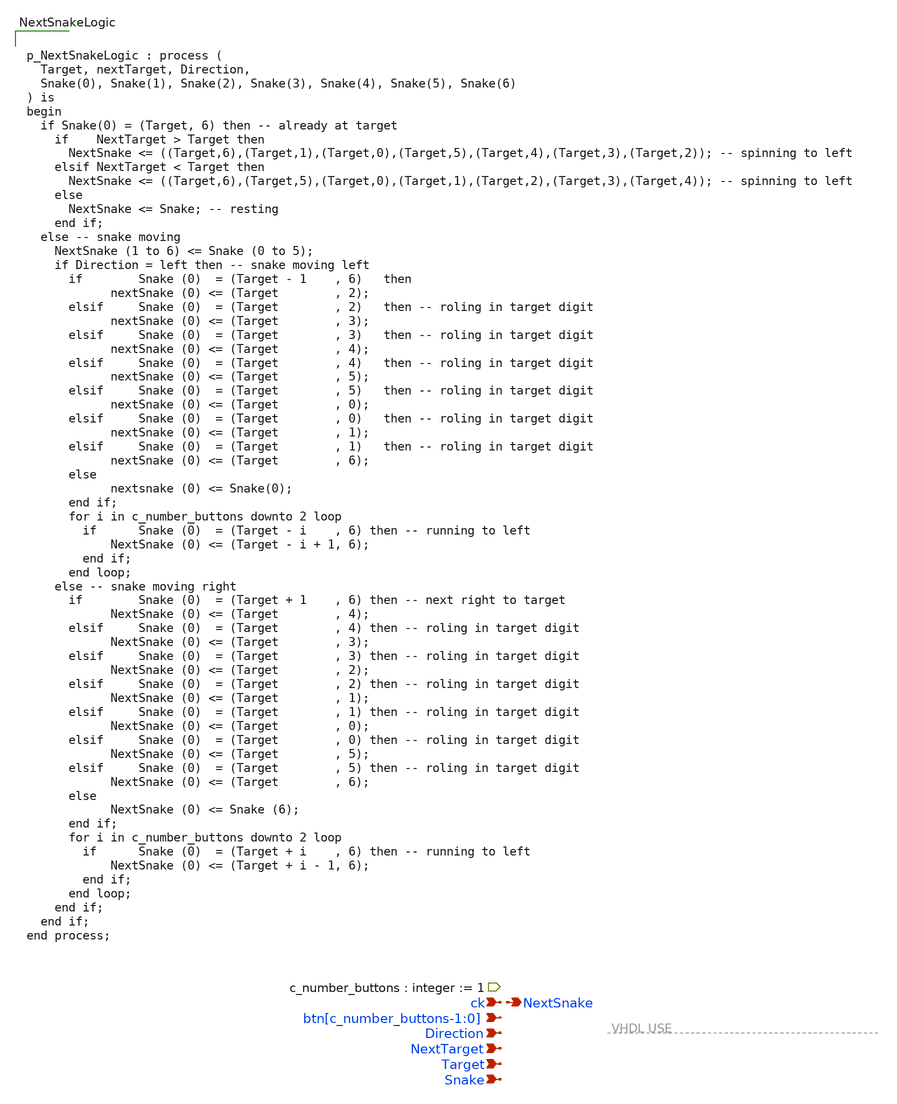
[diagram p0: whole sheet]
** sch_path: xschem/NextSnakeLogic.sch
**.subckt NextSnakeLogic ck NextSnake Snake btn[c_number_buttons-1:0] Target Direction NextTarget
*.ipin ck
*.opin NextSnake
*.ipin Snake
*.ipin btn[c_number_buttons-1:0]
*.ipin Target
*.ipin Direction
*.ipin NextTarget
**** begin user architecture code


p_NextSnakeLogic : process (
  Target, nextTarget, Direction,
  Snake(0), Snake(1), Snake(2), Snake(3), Snake(4), Snake(5), Snake(6)
) is
begin
  if Snake(0) = (Target, 6) then -- already at target
    if    NextTarget > Target then
      NextSnake <= ((Target,6),(Target,1),(Target,0),(Target,5),(Target,4),(Target,3),(Target,2));
+ -- spinning to left
    elsif NextTarget < Target then
      NextSnake <= ((Target,6),(Target,5),(Target,0),(Target,1),(Target,2),(Target,3),(Target,4));
+ -- spinning to left
    else
      NextSnake <= Snake; -- resting
    end if;
  else -- snake moving
    NextSnake (1 to 6) <= Snake (0 to 5);
    if Direction = left then -- snake moving left
      if        Snake (0)  = (Target - 1    , 6)   then
            nextSnake (0) <= (Target        , 2);
      elsif     Snake (0)  = (Target        , 2)   then -- roling in target digit
            nextSnake (0) <= (Target        , 3);
      elsif     Snake (0)  = (Target        , 3)   then -- roling in target digit
            nextSnake (0) <= (Target        , 4);
      elsif     Snake (0)  = (Target        , 4)   then -- roling in target digit
            nextSnake (0) <= (Target        , 5);
      elsif     Snake (0)  = (Target        , 5)   then -- roling in target digit
            nextSnake (0) <= (Target        , 0);
      elsif     Snake (0)  = (Target        , 0)   then -- roling in target digit
            nextSnake (0) <= (Target        , 1);
      elsif     Snake (0)  = (Target        , 1)   then -- roling in target digit
            nextSnake (0) <= (Target        , 6);
      else
            nextsnake (0) <= Snake(0);
      end if;
      for i in c_number_buttons downto 2 loop
        if      Snake (0)  = (Target - i    , 6) then -- running to left
            NextSnake (0) <= (Target - i + 1, 6);
        end if;
      end loop;
    else -- snake moving right
      if        Snake (0)  = (Target + 1    , 6) then -- next right to target
            NextSnake (0) <= (Target        , 4);
      elsif     Snake (0)  = (Target        , 4) then -- roling in target digit
            NextSnake (0) <= (Target        , 3);
      elsif     Snake (0)  = (Target        , 3) then -- roling in target digit
            NextSnake (0) <= (Target        , 2);
      elsif     Snake (0)  = (Target        , 2) then -- roling in target digit
            NextSnake (0) <= (Target        , 1);
      elsif     Snake (0)  = (Target        , 1) then -- roling in target digit
            NextSnake (0) <= (Target        , 0);
      elsif     Snake (0)  = (Target        , 0) then -- roling in target digit
            NextSnake (0) <= (Target        , 5);
      elsif     Snake (0)  = (Target        , 5) then -- roling in target digit
            NextSnake (0) <= (Target        , 6);
      else
            NextSnake (0) <= Snake (6);
      end if;
      for i in c_number_buttons downto 2 loop
        if      Snake (0)  = (Target + i    , 6) then -- running to left
            NextSnake (0) <= (Target + i - 1, 6);
        end if;
      end loop;
    end if;
  end if;
end process;


**** end user architecture code
**.ends
.end
